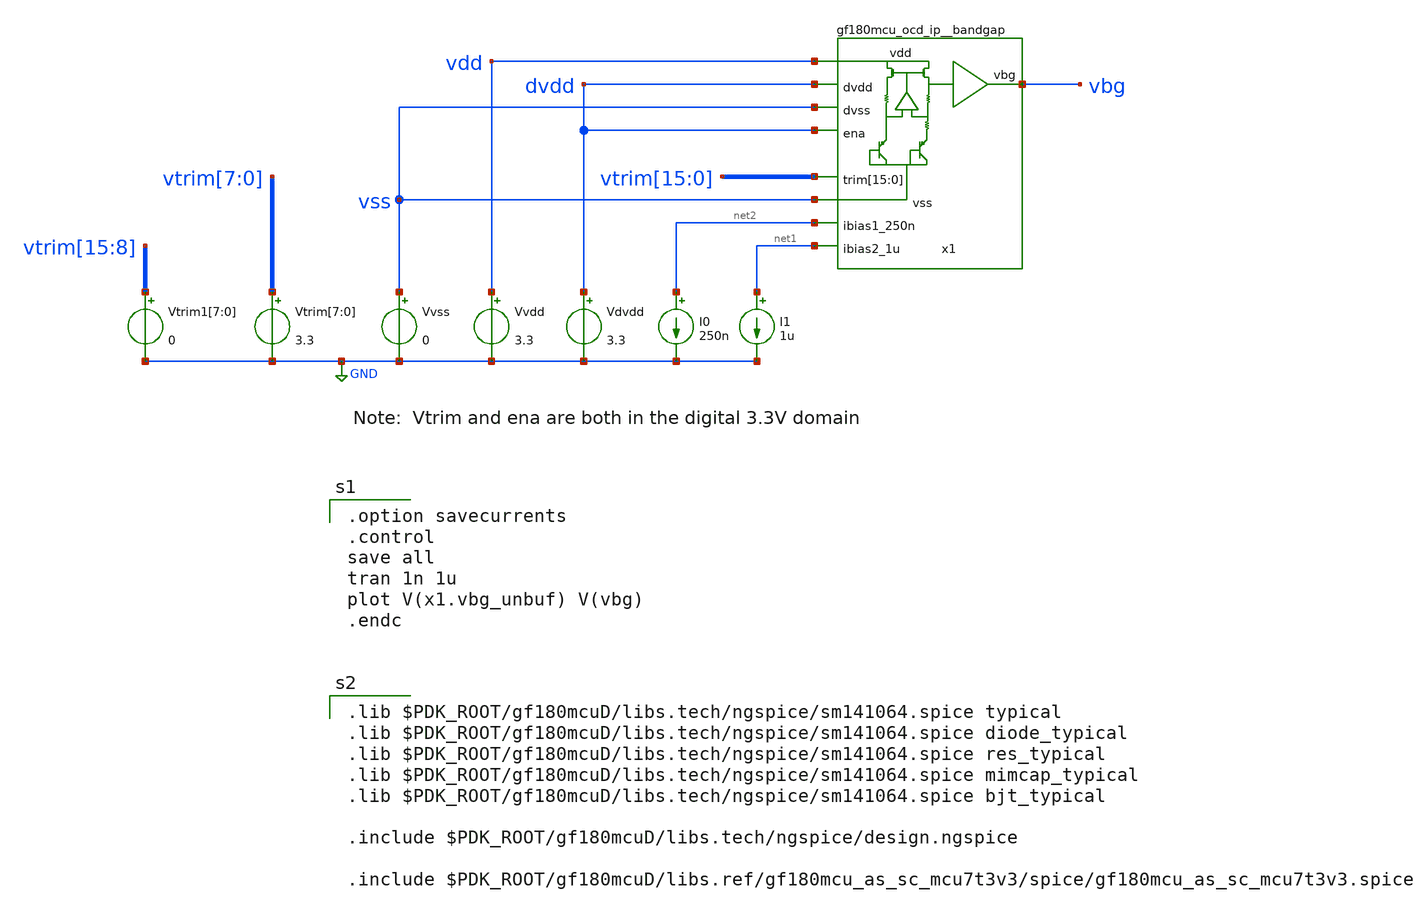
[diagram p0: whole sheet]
** sch_path: xschem/bandgap_tb.sch
**.subckt bandgap_tb
Vvss vss GND 0
Vtrim[7] vtrim[7] GND 3.3
Vtrim[6] vtrim[6] GND 3.3
Vtrim[5] vtrim[5] GND 3.3
Vtrim[4] vtrim[4] GND 3.3
Vtrim[3] vtrim[3] GND 3.3
Vtrim[2] vtrim[2] GND 3.3
Vtrim[1] vtrim[1] GND 3.3
Vtrim[0] vtrim[0] GND 3.3
Vvdd vdd GND 3.3
I0 net2 GND 250n
Vdvdd dvdd GND 3.3
I1 net1 GND 1u
Vtrim1[7] vtrim[15] GND 0
Vtrim1[6] vtrim[14] GND 0
Vtrim1[5] vtrim[13] GND 0
Vtrim1[4] vtrim[12] GND 0
Vtrim1[3] vtrim[11] GND 0
Vtrim1[2] vtrim[10] GND 0
Vtrim1[1] vtrim[9] GND 0
Vtrim1[0] vtrim[8] GND 0
x1 vdd vbg vss net2 vtrim[15] vtrim[14] vtrim[13] vtrim[12] vtrim[11] vtrim[10] vtrim[9] vtrim[8]
+ vtrim[7] vtrim[6] vtrim[5] vtrim[4] vtrim[3] vtrim[2] vtrim[1] vtrim[0] vss dvdd dvdd net1
+ gf180mcu_ocd_ip__bandgap
**** begin user architecture code

.option savecurrents
.control
save all
tran 1n 1u
plot V(x1.vbg_unbuf) V(vbg)
.endc


.lib $PDK_ROOT/gf180mcuD/libs.tech/ngspice/sm141064.spice typical
.lib $PDK_ROOT/gf180mcuD/libs.tech/ngspice/sm141064.spice diode_typical
.lib $PDK_ROOT/gf180mcuD/libs.tech/ngspice/sm141064.spice res_typical
.lib $PDK_ROOT/gf180mcuD/libs.tech/ngspice/sm141064.spice mimcap_typical
.lib $PDK_ROOT/gf180mcuD/libs.tech/ngspice/sm141064.spice bjt_typical

.include $PDK_ROOT/gf180mcuD/libs.tech/ngspice/design.ngspice

.include $PDK_ROOT/gf180mcuD/libs.ref/gf180mcu_as_sc_mcu7t3v3/spice/gf180mcu_as_sc_mcu7t3v3.spice


**** end user architecture code
**.ends
.GLOBAL GND
.end
